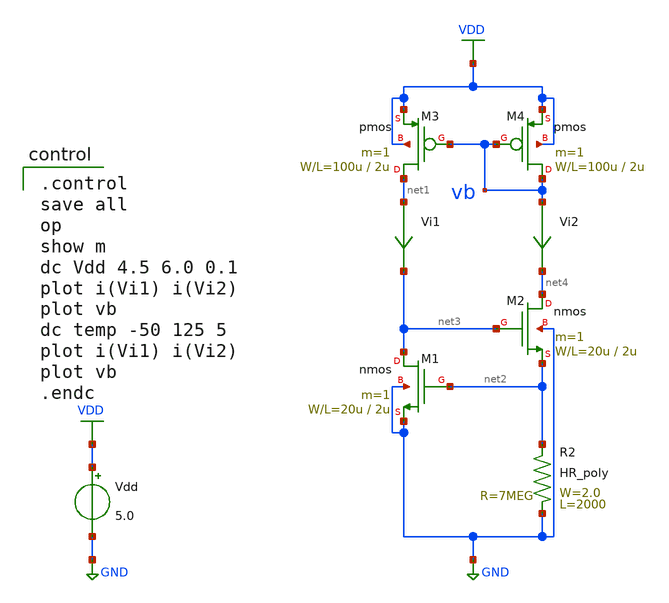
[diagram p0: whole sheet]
** sch_path: OR1/PTC06/current-source/cs-vth-ref.sch
**.subckt cs-vth-ref
Vdd VDD GND 5.0
Vi1 net1 net3 0
.save i(vi1)
Vi2 vb net4 0
.save i(vi2)
R2 GND net2 HR_poly W=2.0 L=2000
M4 vb vb VDD VDD pmos L=2u W=100u m=1
M3 net1 vb VDD VDD pmos L=2u W=100u m=1
M2 net4 net3 net2 GND nmos L=2u W=20u m=1
M1 net3 net2 GND GND nmos L=2u W=20u m=1
**** begin user architecture code

.control
save all
op
show m
dc Vdd 4.5 6.0 0.1
plot i(Vi1) i(Vi2)
plot vb
dc temp -50 125 5
plot i(Vi1) i(Vi2)
plot vb
.endc

 .include $::LIB/mos.lib
.include $::LIB/passive.lib
.include $::LIB/diode.lib
**** end user architecture code
**.ends
.GLOBAL GND
.GLOBAL VDD
.end
